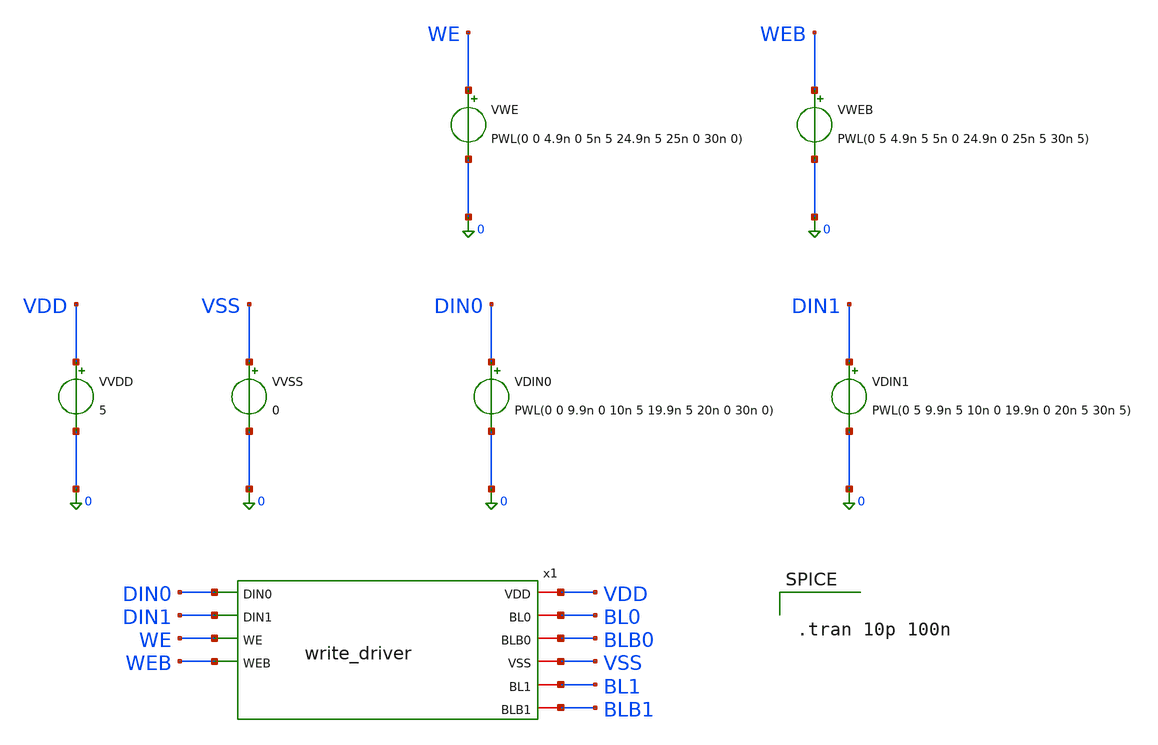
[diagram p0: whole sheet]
** sch_path: Deliverables/tb_write_driver.sch
**.subckt tb_write_driver
x1 DIN0 VDD BL0 BLB0 VSS DIN1 BL1 WE BLB1 WEB write_driver
VVDD VDD 0 5
VVSS VSS 0 0
VDIN0 DIN0 0 PWL(0 0 9.9n 0 10n 5 19.9n 5 20n 0 30n 0)
VDIN1 DIN1 0 PWL(0 5 9.9n 5 10n 0 19.9n 0 20n 5 30n 5)
VWE WE 0 PWL(0 0 4.9n 0 5n 5 24.9n 5 25n 0 30n 0)
VWEB WEB 0 PWL(0 5 4.9n 5 5n 0 24.9n 0 25n 5 30n 5)
**** begin user architecture code
 .include $::LIB/ip62_models


.tran 10p 100n



**** end user architecture code
**.ends
.end
